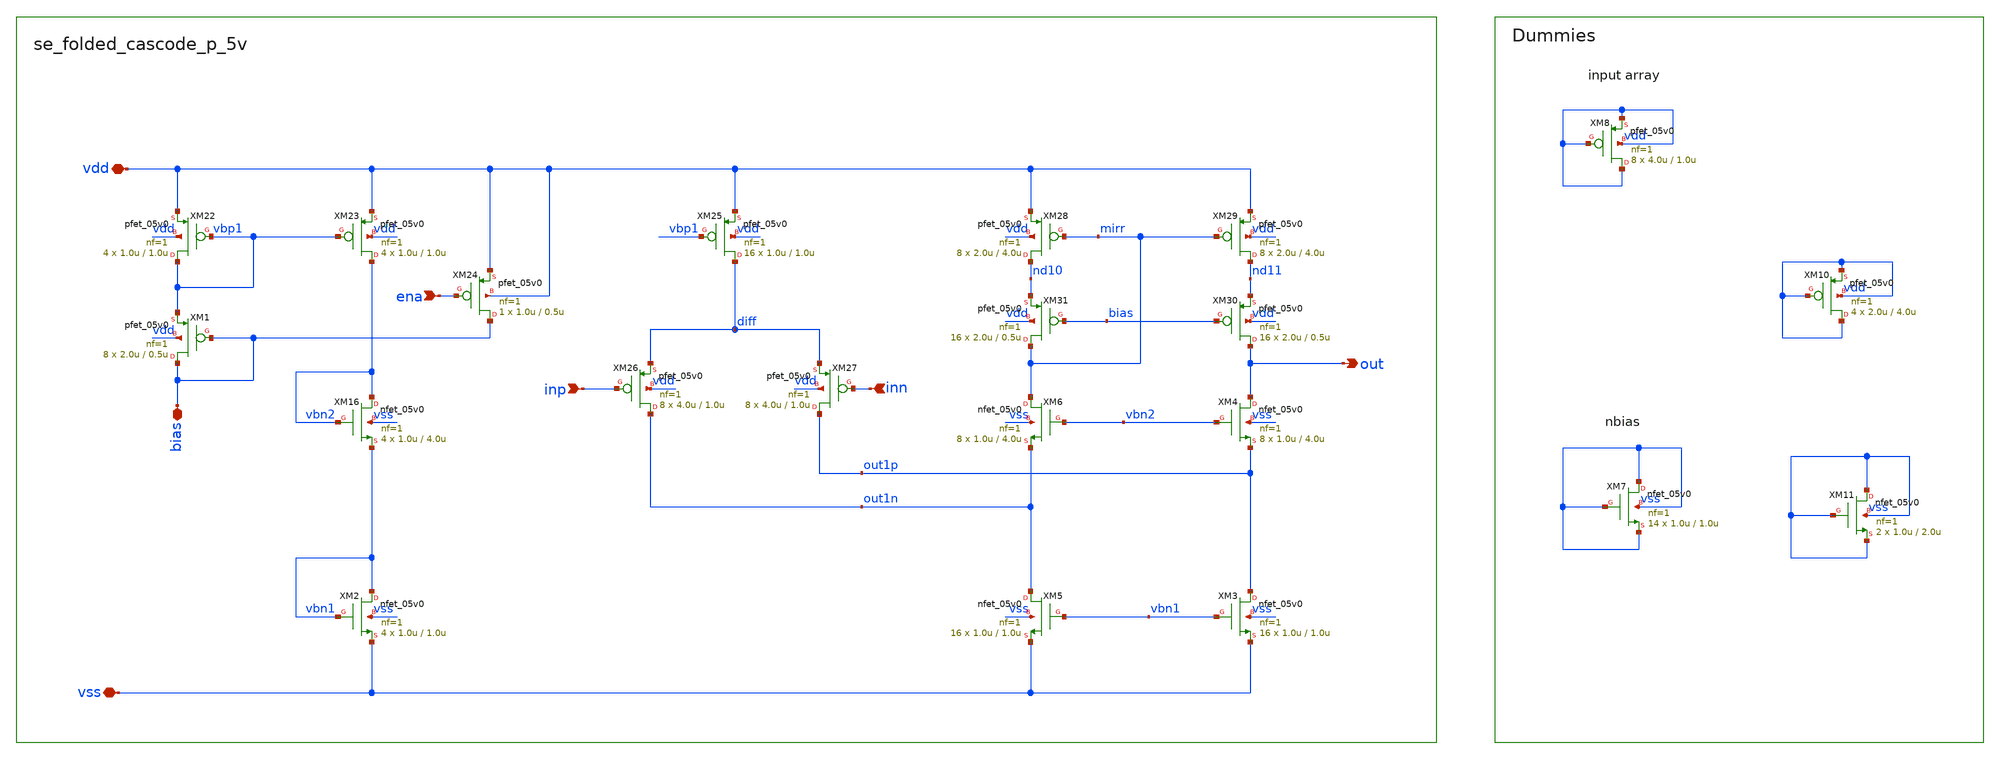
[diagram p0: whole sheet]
** sch_path: xschem/se_folded_cascode_p_5v.sch
**.subckt se_folded_cascode_p_5v inn inp out bias vdd vss ena
*.ipin inn
*.ipin inp
*.opin out
*.iopin bias
*.iopin vdd
*.iopin vss
*.ipin ena
XM16 vbn2 vbn2 vbn1 vss nfet_05v0 L=4.0u W=1.0u nf=1 ad='int((nf+1)/2) * W/nf * 0.18u' as='int((nf+2)/2) * W/nf * 0.18u'
+ pd='2*int((nf+1)/2) * (W/nf + 0.18u)' ps='2*int((nf+2)/2) * (W/nf + 0.18u)' nrd='0.18u / W' nrs='0.18u / W'
+ sa=0 sb=0 sd=0 m=4
XM22 vbp1 vbp1 vdd vdd pfet_05v0 L=1.0u W=1.0u nf=1 ad='int((nf+1)/2) * W/nf * 0.18u' as='int((nf+2)/2) * W/nf * 0.18u'
+ pd='2*int((nf+1)/2) * (W/nf + 0.18u)' ps='2*int((nf+2)/2) * (W/nf + 0.18u)' nrd='0.18u / W' nrs='0.18u / W'
+ sa=0 sb=0 sd=0 m=4 par=4
XM23 vbn2 vbp1 vdd vdd pfet_05v0 L=1.0u W=1.0u nf=1 ad='int((nf+1)/2) * W/nf * 0.18u' as='int((nf+2)/2) * W/nf * 0.18u'
+ pd='2*int((nf+1)/2) * (W/nf + 0.18u)' ps='2*int((nf+2)/2) * (W/nf + 0.18u)' nrd='0.18u / W' nrs='0.18u / W'
+ sa=0 sb=0 sd=0 m=4 par=4
XM24 bias ena vdd vdd pfet_05v0 L=0.5u W=1.0u nf=1 ad='int((nf+1)/2) * W/nf * 0.18u' as='int((nf+2)/2) * W/nf * 0.18u'
+ pd='2*int((nf+1)/2) * (W/nf + 0.18u)' ps='2*int((nf+2)/2) * (W/nf + 0.18u)' nrd='0.18u / W' nrs='0.18u / W'
+ sa=0 sb=0 sd=0 m=1 par=1
XM25 diff vbp1 vdd vdd pfet_05v0 L=1.0u W=1.0u nf=1 ad='int((nf+1)/2) * W/nf * 0.18u' as='int((nf+2)/2) * W/nf * 0.18u'
+ pd='2*int((nf+1)/2) * (W/nf + 0.18u)' ps='2*int((nf+2)/2) * (W/nf + 0.18u)' nrd='0.18u / W' nrs='0.18u / W'
+ sa=0 sb=0 sd=0 m=16 par=16
XM26 out1n inp diff vdd pfet_05v0 L=1.0u W=4.0u nf=1 ad='int((nf+1)/2) * W/nf * 0.18u' as='int((nf+2)/2) * W/nf * 0.18u'
+ pd='2*int((nf+1)/2) * (W/nf + 0.18u)' ps='2*int((nf+2)/2) * (W/nf + 0.18u)' nrd='0.18u / W' nrs='0.18u / W'
+ sa=0 sb=0 sd=0 m=8 par=8
XM27 out1p inn diff vdd pfet_05v0 L=1.0u W=4.0u nf=1 ad='int((nf+1)/2) * W/nf * 0.18u' as='int((nf+2)/2) * W/nf * 0.18u'
+ pd='2*int((nf+1)/2) * (W/nf + 0.18u)' ps='2*int((nf+2)/2) * (W/nf + 0.18u)' nrd='0.18u / W' nrs='0.18u / W'
+ sa=0 sb=0 sd=0 m=8 par=8
XM28 nd10 mirr vdd vdd pfet_05v0 L=4.0u W=2.0u nf=1 ad='int((nf+1)/2) * W/nf * 0.18u' as='int((nf+2)/2) * W/nf * 0.18u'
+ pd='2*int((nf+1)/2) * (W/nf + 0.18u)' ps='2*int((nf+2)/2) * (W/nf + 0.18u)' nrd='0.18u / W' nrs='0.18u / W'
+ sa=0 sb=0 sd=0 m=8 par=8
XM29 nd11 mirr vdd vdd pfet_05v0 L=4.0u W=2.0u nf=1 ad='int((nf+1)/2) * W/nf * 0.18u' as='int((nf+2)/2) * W/nf * 0.18u'
+ pd='2*int((nf+1)/2) * (W/nf + 0.18u)' ps='2*int((nf+2)/2) * (W/nf + 0.18u)' nrd='0.18u / W' nrs='0.18u / W'
+ sa=0 sb=0 sd=0 m=8 par=8
XM30 out bias nd11 vdd pfet_05v0 L=0.5u W=2.0u nf=1 ad='int((nf+1)/2) * W/nf * 0.18u' as='int((nf+2)/2) * W/nf * 0.18u'
+ pd='2*int((nf+1)/2) * (W/nf + 0.18u)' ps='2*int((nf+2)/2) * (W/nf + 0.18u)' nrd='0.18u / W' nrs='0.18u / W'
+ sa=0 sb=0 sd=0 m=16 par=16
XM31 mirr bias nd10 vdd pfet_05v0 L=0.5u W=2.0u nf=1 ad='int((nf+1)/2) * W/nf * 0.18u' as='int((nf+2)/2) * W/nf * 0.18u'
+ pd='2*int((nf+1)/2) * (W/nf + 0.18u)' ps='2*int((nf+2)/2) * (W/nf + 0.18u)' nrd='0.18u / W' nrs='0.18u / W'
+ sa=0 sb=0 sd=0 m=16 par=16
XM1 bias bias vbp1 vdd pfet_05v0 L=0.5u W=2.0u nf=1 ad='int((nf+1)/2) * W/nf * 0.18u' as='int((nf+2)/2) * W/nf * 0.18u'
+ pd='2*int((nf+1)/2) * (W/nf + 0.18u)' ps='2*int((nf+2)/2) * (W/nf + 0.18u)' nrd='0.18u / W' nrs='0.18u / W'
+ sa=0 sb=0 sd=0 m=8 par=8
XM2 vbn1 vbn1 vss vss nfet_05v0 L=1.0u W=1.0u nf=1 ad='int((nf+1)/2) * W/nf * 0.18u' as='int((nf+2)/2) * W/nf * 0.18u'
+ pd='2*int((nf+1)/2) * (W/nf + 0.18u)' ps='2*int((nf+2)/2) * (W/nf + 0.18u)' nrd='0.18u / W' nrs='0.18u / W'
+ sa=0 sb=0 sd=0 m=4
XM3 out1p vbn1 vss vss nfet_05v0 L=1.0u W=1.0u nf=1 ad='int((nf+1)/2) * W/nf * 0.18u' as='int((nf+2)/2) * W/nf * 0.18u'
+ pd='2*int((nf+1)/2) * (W/nf + 0.18u)' ps='2*int((nf+2)/2) * (W/nf + 0.18u)' nrd='0.18u / W' nrs='0.18u / W'
+ sa=0 sb=0 sd=0 m=16
XM5 out1n vbn1 vss vss nfet_05v0 L=1.0u W=1.0u nf=1 ad='int((nf+1)/2) * W/nf * 0.18u' as='int((nf+2)/2) * W/nf * 0.18u'
+ pd='2*int((nf+1)/2) * (W/nf + 0.18u)' ps='2*int((nf+2)/2) * (W/nf + 0.18u)' nrd='0.18u / W' nrs='0.18u / W'
+ sa=0 sb=0 sd=0 m=16
XM6 mirr vbn2 out1n vss nfet_05v0 L=4.0u W=1.0u nf=1 ad='int((nf+1)/2) * W/nf * 0.18u' as='int((nf+2)/2) * W/nf * 0.18u'
+ pd='2*int((nf+1)/2) * (W/nf + 0.18u)' ps='2*int((nf+2)/2) * (W/nf + 0.18u)' nrd='0.18u / W' nrs='0.18u / W'
+ sa=0 sb=0 sd=0 m=8
XM4 out vbn2 out1p vss nfet_05v0 L=4.0u W=1.0u nf=1 ad='int((nf+1)/2) * W/nf * 0.18u' as='int((nf+2)/2) * W/nf * 0.18u'
+ pd='2*int((nf+1)/2) * (W/nf + 0.18u)' ps='2*int((nf+2)/2) * (W/nf + 0.18u)' nrd='0.18u / W' nrs='0.18u / W'
+ sa=0 sb=0 sd=0 m=8
XM7 vss vss vss vss nfet_05v0 L=1.0u W=1.0u nf=1 ad='int((nf+1)/2) * W/nf * 0.18u' as='int((nf+2)/2) * W/nf * 0.18u'
+ pd='2*int((nf+1)/2) * (W/nf + 0.18u)' ps='2*int((nf+2)/2) * (W/nf + 0.18u)' nrd='0.18u / W' nrs='0.18u / W'
+ sa=0 sb=0 sd=0 m=14
XM8 vdd vdd vdd vdd pfet_05v0 L=1.0u W=4.0u nf=1 ad='int((nf+1)/2) * W/nf * 0.18u' as='int((nf+2)/2) * W/nf * 0.18u'
+ pd='2*int((nf+1)/2) * (W/nf + 0.18u)' ps='2*int((nf+2)/2) * (W/nf + 0.18u)' nrd='0.18u / W' nrs='0.18u / W'
+ sa=0 sb=0 sd=0 m=8 par=8
XM10 vdd vdd vdd vdd pfet_05v0 L=4.0u W=2.0u nf=1 ad='int((nf+1)/2) * W/nf * 0.18u' as='int((nf+2)/2) * W/nf * 0.18u'
+ pd='2*int((nf+1)/2) * (W/nf + 0.18u)' ps='2*int((nf+2)/2) * (W/nf + 0.18u)' nrd='0.18u / W' nrs='0.18u / W'
+ sa=0 sb=0 sd=0 m=4 par=4
XM11 vss vss vss vss nfet_05v0 L=2.0u W=1.0u nf=1 ad='int((nf+1)/2) * W/nf * 0.18u' as='int((nf+2)/2) * W/nf * 0.18u'
+ pd='2*int((nf+1)/2) * (W/nf + 0.18u)' ps='2*int((nf+2)/2) * (W/nf + 0.18u)' nrd='0.18u / W' nrs='0.18u / W'
+ sa=0 sb=0 sd=0 m=2
**.ends
.end
